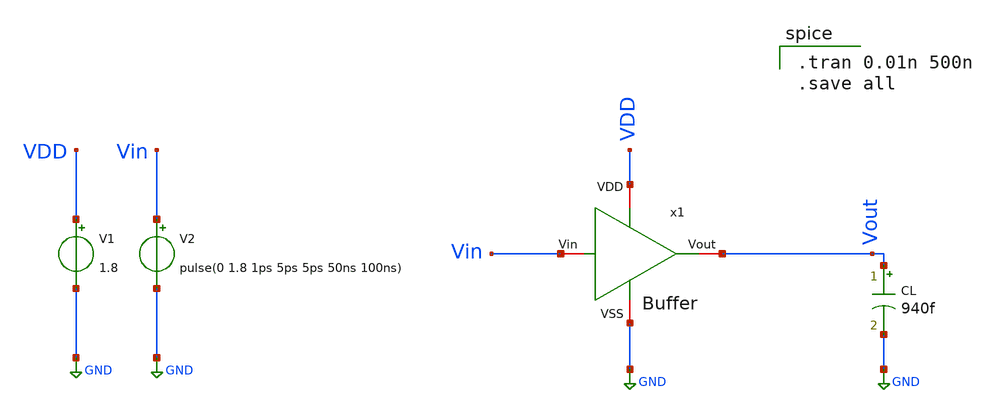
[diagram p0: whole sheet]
** sch_path: TB/Buffer_TB.sch
**.subckt Buffer_TB
V1 VDD GND 1.8
V2 Vin GND pulse(0 1.8 1ps 5ps 5ps 50ns 100ns)
CL Vout GND 940f m=1
x1 VDD GND Vin Vout Buffer
**** begin user architecture code

.tran 0.01n 500n
.save all

 .lib $::SKYWATER_MODELS/sky130.lib.spice tt
.include $::SKYWATER_STDCELLS/sky130_fd_sc_hd.spice

**** end user architecture code
**.ends

* expanding   symbol:  /foss/designs/RO_Aging_UNICASS/Buffer/Buffer.sym # of pins=4
** sym_path: Buffer/Buffer.sym
** sch_path: Buffer/Buffer.sch
.subckt Buffer VDD VSS Vin Vout
*.iopin VDD
*.iopin Vin
*.iopin Vout
*.iopin VSS
XM1 net1 Vin VSS VSS sky130_fd_pr__nfet_01v8 L=0.15 W=1 nf=1 ad='int((nf+1)/2) * W/nf * 0.29' as='int((nf+2)/2) * W/nf * 0.29'
+ pd='2*int((nf+1)/2) * (W/nf + 0.29)' ps='2*int((nf+2)/2) * (W/nf + 0.29)' nrd='0.29 / W' nrs='0.29 / W'
+ sa=0 sb=0 sd=0 mult=1 m=1
XM2 net1 Vin VDD VDD sky130_fd_pr__pfet_01v8 L=0.15 W=1 nf=1 ad='int((nf+1)/2) * W/nf * 0.29' as='int((nf+2)/2) * W/nf * 0.29'
+ pd='2*int((nf+1)/2) * (W/nf + 0.29)' ps='2*int((nf+2)/2) * (W/nf + 0.29)' nrd='0.29 / W' nrs='0.29 / W'
+ sa=0 sb=0 sd=0 mult=1 m=1
XM3 Vout net1 VSS VSS sky130_fd_pr__nfet_01v8 L=0.15 W=1 nf=1 ad='int((nf+1)/2) * W/nf * 0.29' as='int((nf+2)/2) * W/nf * 0.29'
+ pd='2*int((nf+1)/2) * (W/nf + 0.29)' ps='2*int((nf+2)/2) * (W/nf + 0.29)' nrd='0.29 / W' nrs='0.29 / W'
+ sa=0 sb=0 sd=0 mult=4 m=4
XM4 Vout net1 VDD VDD sky130_fd_pr__pfet_01v8 L=0.15 W=1 nf=1 ad='int((nf+1)/2) * W/nf * 0.29' as='int((nf+2)/2) * W/nf * 0.29'
+ pd='2*int((nf+1)/2) * (W/nf + 0.29)' ps='2*int((nf+2)/2) * (W/nf + 0.29)' nrd='0.29 / W' nrs='0.29 / W'
+ sa=0 sb=0 sd=0 mult=4 m=4
.ends

.GLOBAL GND
.end
